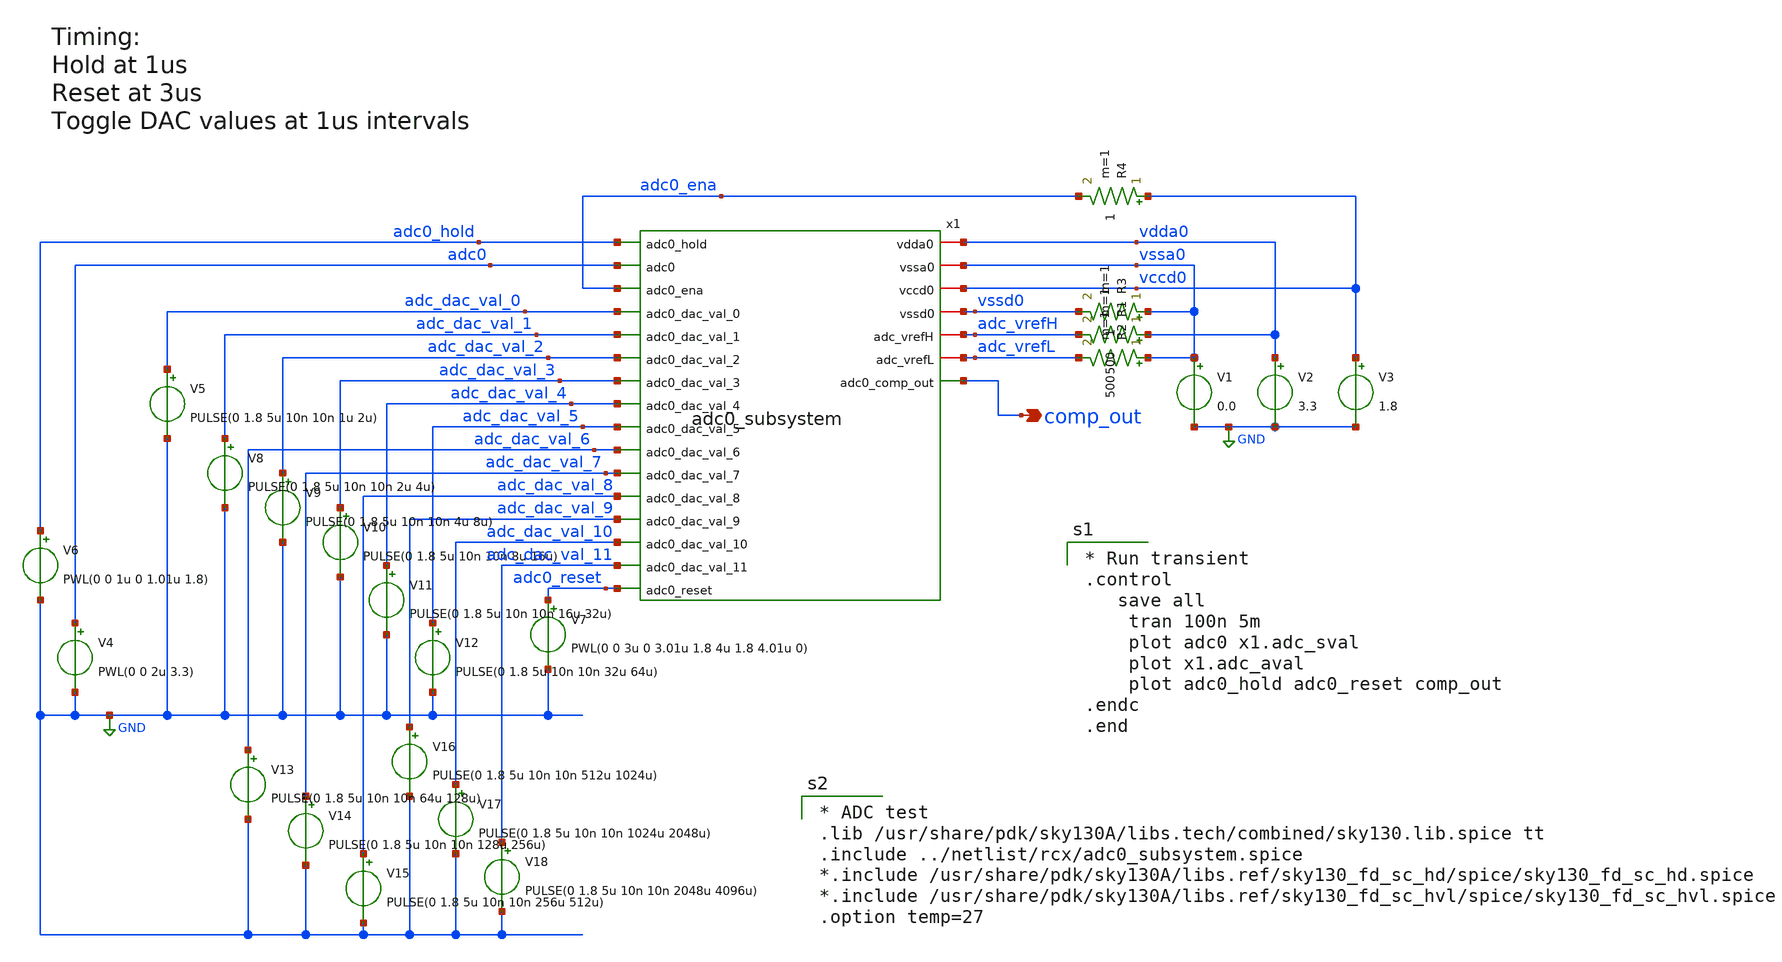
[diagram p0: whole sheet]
** sch_path: cace/adc_calibration_tb.sch
**.subckt adc_calibration_tb comp_out
*.opin comp_out
x1 vdda0 vssa0 vccd0 vssd0 adc_vrefH adc_vrefL adc0_hold adc0 adc0_ena adc_dac_val_0 adc_dac_val_1
+ adc_dac_val_2 adc_dac_val_3 comp_out adc_dac_val_4 adc_dac_val_5 adc_dac_val_6 adc_dac_val_7 adc_dac_val_8
+ adc_dac_val_9 adc_dac_val_10 adc_dac_val_11 adc0_reset adc0_subsystem
V1 vssa0 GND 0.0
V2 vdda0 GND 3.3
V3 vccd0 GND 1.8
V4 adc0 GND PWL(0 0 2u 3.3)
V5 adc_dac_val_0 GND PULSE(0 1.8 5u 10n 10n 1u 2u)
V6 adc0_hold GND PWL(0 0 1u 0 1.01u 1.8)
V7 adc0_reset GND PWL(0 0 3u 0 3.01u 1.8 4u 1.8 4.01u 0)
V8 adc_dac_val_1 GND PULSE(0 1.8 5u 10n 10n 2u 4u)
V9 adc_dac_val_2 GND PULSE(0 1.8 5u 10n 10n 4u 8u)
V10 adc_dac_val_3 GND PULSE(0 1.8 5u 10n 10n 8u 16u)
V11 adc_dac_val_4 GND PULSE(0 1.8 5u 10n 10n 16u 32u)
V12 adc_dac_val_5 GND PULSE(0 1.8 5u 10n 10n 32u 64u)
V13 adc_dac_val_6 GND PULSE(0 1.8 5u 10n 10n 64u 128u)
V14 adc_dac_val_7 GND PULSE(0 1.8 5u 10n 10n 128u 256u)
V15 adc_dac_val_8 GND PULSE(0 1.8 5u 10n 10n 256u 512u)
V16 adc_dac_val_9 GND PULSE(0 1.8 5u 10n 10n 512u 1024u)
V17 adc_dac_val_10 GND PULSE(0 1.8 5u 10n 10n 1024u 2048u)
V18 adc_dac_val_11 GND PULSE(0 1.8 5u 10n 10n 2048u 4096u)
R1 vdda0 adc_vrefH 500 m=1
R2 vssa0 adc_vrefL 500 m=1
R3 vssa0 vssd0 1 m=1
R4 vccd0 adc0_ena 1 m=1
**** begin user architecture code

* Run transient
.control
   save all
    tran 100n 5m
    plot adc0 x1.adc_sval
    plot x1.adc_aval
    plot adc0_hold adc0_reset comp_out
.endc
.end


* ADC test
.lib /usr/share/pdk/sky130A/libs.tech/combined/sky130.lib.spice tt
.include ../netlist/rcx/adc0_subsystem.spice
*.include /usr/share/pdk/sky130A/libs.ref/sky130_fd_sc_hd/spice/sky130_fd_sc_hd.spice
*.include /usr/share/pdk/sky130A/libs.ref/sky130_fd_sc_hvl/spice/sky130_fd_sc_hvl.spice
.option temp=27

**** end user architecture code
**.ends
.GLOBAL GND
.end
